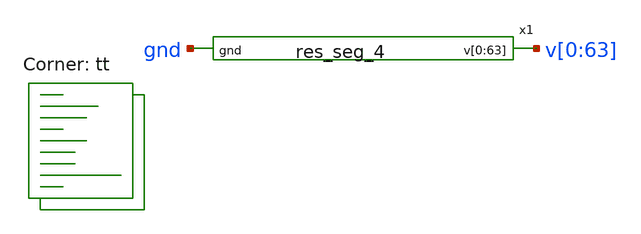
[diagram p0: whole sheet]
** sch_path: xschem/res_seg_4-tb.sch
**.subckt res_seg_4-tb
x1 v[0] v[1] v[2] v[3] v[4] v[5] v[6] v[7] v[8] v[9] v[10] v[11] v[12] v[13] v[14] v[15] v[16] v[17]
+ v[18] v[19] v[20] v[21] v[22] v[23] v[24] v[25] v[26] v[27] v[28] v[29] v[30] v[31] v[32] v[33] v[34]
+ v[35] v[36] v[37] v[38] v[39] v[40] v[41] v[42] v[43] v[44] v[45] v[46] v[47] v[48] v[49] v[50] v[51]
+ v[52] v[53] v[54] v[55] v[56] v[57] v[58] v[59] v[60] v[61] v[62] v[63] gnd res_seg_4
**** begin user architecture code



  .param max_freq=500e3 period={1/max_freq} time_high={period/2}
  .param delay_vin1={time_high} delay_vin2={time_high*1.5}
  .param lval=100u

  .option wnflag=1
  .option safecurrents

  V63 v[63] gnd dc 5
  v0 v[0] gnd dc 4.2182
  *Vin  in  gnd pulse(0 1.8 {delay_vin1} 1p 1p {time_high} {period})
  *Vinb inb gnd pulse(1.8 0 {delay_vin1} 1p 1p {time_high} {period})

  .control
     reset
     save all
     tran 1p 1n
     write res_seg_4-tb.raw
     set appendwrite

     *reset
     *save all
     *dc vref 0 1.8 0.1
     *write lvsf-tb.raw
*    quit 0
  .endc



.lib $::SKYWATER_MODELS/sky130.lib.spice tt
**** end user architecture code
**.ends

* expanding   symbol:  res_seg_4.sym # of pins=2
** sym_path: xschem/res_seg_4.sym
** sch_path: xschem/res_seg_4.sch
.subckt res_seg_4 v[0] v[1] v[2] v[3] v[4] v[5] v[6] v[7] v[8] v[9] v[10] v[11] v[12] v[13] v[14]
+ v[15] v[16] v[17] v[18] v[19] v[20] v[21] v[22] v[23] v[24] v[25] v[26] v[27] v[28] v[29] v[30] v[31]
+ v[32] v[33] v[34] v[35] v[36] v[37] v[38] v[39] v[40] v[41] v[42] v[43] v[44] v[45] v[46] v[47] v[48]
+ v[49] v[50] v[51] v[52] v[53] v[54] v[55] v[56] v[57] v[58] v[59] v[60] v[61] v[62] v[63] gnd
*.opin
*+ v[0],v[1],v[2],v[3],v[4],v[5],v[6],v[7],v[8],v[9],v[10],v[11],v[12],v[13],v[14],v[15],v[16],v[17],v[18],v[19],v[20],v[21],v[22],v[23],v[24],v[25],v[26],v[27],v[28],v[29],v[30],v[31],v[32],v[33],v[34],v[35],v[36],v[37],v[38],v[39],v[40],v[41],v[42],v[43],v[44],v[45],v[46],v[47],v[48],v[49],v[50],v[51],v[52],v[53],v[54],v[55],v[56],v[57],v[58],v[59],v[60],v[61],v[62],v[63]
*.ipin gnd
XR1 v[0] v[1] gnd sky130_fd_pr__res_xhigh_po_2p85 L=0.9742 mult=1 m=1
XR2 v[1] v[2] gnd sky130_fd_pr__res_xhigh_po_1p41 L=0.5164 mult=1 m=1
XR3 v[2] v[3] gnd sky130_fd_pr__res_xhigh_po_1p41 L=0.5164 mult=1 m=1
XR4 v[3] v[4] gnd sky130_fd_pr__res_xhigh_po_2p85 L=0.9742 mult=1 m=1
XR5 v[4] v[5] gnd sky130_fd_pr__res_xhigh_po_1p41 L=0.5164 mult=1 m=1
XR6 v[5] v[6] gnd sky130_fd_pr__res_xhigh_po_1p41 L=0.5164 mult=1 m=1
XR7 v[6] v[7] gnd sky130_fd_pr__res_xhigh_po_1p41 L=0.5508 mult=1 m=1
XR8 v[7] v[8] gnd sky130_fd_pr__res_xhigh_po_1p41 L=0.5164 mult=1 m=1
XR9 v[8] v[9] gnd sky130_fd_pr__res_xhigh_po_1p41 L=0.5508 mult=1 m=1
XR10 v[9] v[10] gnd sky130_fd_pr__res_xhigh_po_1p41 L=0.5164 mult=1 m=1
XR11 v[10] v[11] gnd sky130_fd_pr__res_xhigh_po_1p41 L=0.5508 mult=1 m=1
XR12 v[11] v[12] gnd sky130_fd_pr__res_xhigh_po_1p41 L=0.5508 mult=1 m=1
XR13 v[12] v[13] gnd sky130_fd_pr__res_xhigh_po_1p41 L=0.5508 mult=1 m=1
XR14 v[13] v[14] gnd sky130_fd_pr__res_xhigh_po_1p41 L=0.5853 mult=1 m=1
XR15 v[14] v[15] gnd sky130_fd_pr__res_xhigh_po_1p41 L=0.5508 mult=1 m=1
XR16 v[15] v[16] gnd sky130_fd_pr__res_xhigh_po_1p41 L=0.5853 mult=1 m=1
XR17 v[16] v[17] gnd sky130_fd_pr__res_xhigh_po_1p41 L=0.5853 mult=1 m=1
XR18 v[17] v[18] gnd sky130_fd_pr__res_xhigh_po_1p41 L=0.5853 mult=1 m=1
XR19 v[18] v[19] gnd sky130_fd_pr__res_xhigh_po_1p41 L=0.5853 mult=1 m=1
XR20 v[19] v[20] gnd sky130_fd_pr__res_xhigh_po_1p41 L=0.6197 mult=1 m=1
XR21 v[20] v[21] gnd sky130_fd_pr__res_xhigh_po_1p41 L=0.5853 mult=1 m=1
XR22 v[21] v[22] gnd sky130_fd_pr__res_xhigh_po_1p41 L=0.6197 mult=1 m=1
XR23 v[22] v[23] gnd sky130_fd_pr__res_xhigh_po_1p41 L=0.6197 mult=1 m=1
XR24 v[23] v[24] gnd sky130_fd_pr__res_xhigh_po_1p41 L=0.6541 mult=1 m=1
XR25 v[24] v[25] gnd sky130_fd_pr__res_xhigh_po_1p41 L=0.6197 mult=1 m=1
XR26 v[25] v[26] gnd sky130_fd_pr__res_xhigh_po_1p41 L=0.6541 mult=1 m=1
XR27 v[26] v[27] gnd sky130_fd_pr__res_xhigh_po_1p41 L=0.6541 mult=1 m=1
XR28 v[27] v[28] gnd sky130_fd_pr__res_xhigh_po_1p41 L=0.6885 mult=1 m=1
XR29 v[28] v[29] gnd sky130_fd_pr__res_xhigh_po_1p41 L=0.6885 mult=1 m=1
XR30 v[29] v[30] gnd sky130_fd_pr__res_xhigh_po_1p41 L=0.6885 mult=1 m=1
XR31 v[30] v[31] gnd sky130_fd_pr__res_xhigh_po_1p41 L=0.6885 mult=1 m=1
XR32 v[31] v[32] gnd sky130_fd_pr__res_xhigh_po_1p41 L=0.723 mult=1 m=1
XR33 v[32] v[33] gnd sky130_fd_pr__res_xhigh_po_1p41 L=0.723 mult=1 m=1
XR34 v[33] v[34] gnd sky130_fd_pr__res_xhigh_po_1p41 L=0.723 mult=1 m=1
XR35 v[34] v[35] gnd sky130_fd_pr__res_xhigh_po_1p41 L=0.7574 mult=1 m=1
XR36 v[35] v[36] gnd sky130_fd_pr__res_xhigh_po_1p41 L=0.7574 mult=1 m=1
XR37 v[36] v[37] gnd sky130_fd_pr__res_xhigh_po_1p41 L=0.7574 mult=1 m=1
XR38 v[37] v[38] gnd sky130_fd_pr__res_xhigh_po_1p41 L=0.7918 mult=1 m=1
XR39 v[38] v[39] gnd sky130_fd_pr__res_xhigh_po_1p41 L=0.8263 mult=1 m=1
XR40 v[39] v[40] gnd sky130_fd_pr__res_xhigh_po_1p41 L=0.8263 mult=1 m=1
XR41 v[40] v[41] gnd sky130_fd_pr__res_xhigh_po_1p41 L=0.8263 mult=1 m=1
XR42 v[41] v[42] gnd sky130_fd_pr__res_xhigh_po_1p41 L=0.8607 mult=1 m=1
XR43 v[42] v[43] gnd sky130_fd_pr__res_xhigh_po_1p41 L=0.8951 mult=1 m=1
XR44 v[43] v[44] gnd sky130_fd_pr__res_xhigh_po_1p41 L=0.8951 mult=1 m=1
XR45 v[44] v[45] gnd sky130_fd_pr__res_xhigh_po_1p41 L=0.9295 mult=1 m=1
XR46 v[45] v[46] gnd sky130_fd_pr__res_xhigh_po_1p41 L=0.964 mult=1 m=1
XR47 v[46] v[47] gnd sky130_fd_pr__res_xhigh_po_1p41 L=0.964 mult=1 m=1
XR48 v[47] v[48] gnd sky130_fd_pr__res_xhigh_po_1p41 L=0.9984 mult=1 m=1
XR49 v[48] v[49] gnd sky130_fd_pr__res_xhigh_po_0p69 L=0.5223 mult=1 m=1
XR50 v[49] v[50] gnd sky130_fd_pr__res_xhigh_po_0p69 L=0.5223 mult=1 m=1
XR51 v[50] v[51] gnd sky130_fd_pr__res_xhigh_po_0p69 L=0.5391 mult=1 m=1
XR52 v[51] v[52] gnd sky130_fd_pr__res_xhigh_po_0p69 L=0.556 mult=1 m=1
XR53 v[52] v[53] gnd sky130_fd_pr__res_xhigh_po_0p69 L=0.5897 mult=1 m=1
XR54 v[53] v[54] gnd sky130_fd_pr__res_xhigh_po_0p69 L=0.6234 mult=1 m=1
XR55 v[54] v[55] gnd sky130_fd_pr__res_xhigh_po_0p69 L=0.6402 mult=1 m=1
XR56 v[55] v[56] gnd sky130_fd_pr__res_xhigh_po_0p69 L=0.6739 mult=1 m=1
XR57 v[56] v[57] gnd sky130_fd_pr__res_xhigh_po_0p69 L=0.7076 mult=1 m=1
XR58 v[57] v[58] gnd sky130_fd_pr__res_xhigh_po_0p69 L=0.775 mult=1 m=1
XR59 v[58] v[59] gnd sky130_fd_pr__res_xhigh_po_0p69 L=0.8087 mult=1 m=1
XR60 v[59] v[60] gnd sky130_fd_pr__res_xhigh_po_0p69 L=0.8929 mult=1 m=1
XR61 v[60] v[61] gnd sky130_fd_pr__res_xhigh_po_0p69 L=0.9603 mult=1 m=1
XR62 v[61] v[62] gnd sky130_fd_pr__res_xhigh_po_0p35 L=0.5555 mult=1 m=1
XR63 v[62] v[63] gnd sky130_fd_pr__res_xhigh_po_0p35 L=0.6409 mult=1 m=1
.ends

.end
